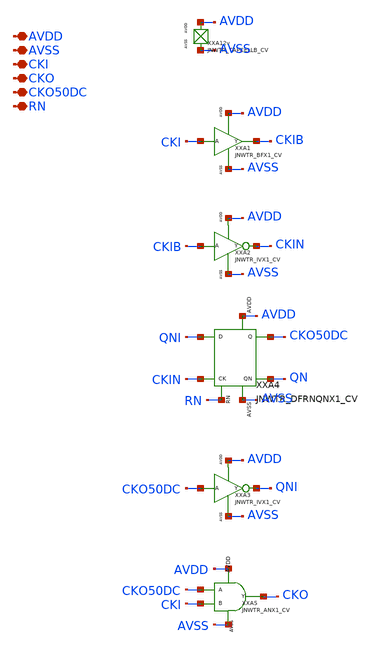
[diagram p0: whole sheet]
** sch_path: design/JNW_TR_SKY130A/JNWTR_CKDIV2_CV.sch
**.subckt JNWTR_CKDIV2_CV AVDD AVSS CKI CKO CKO50DC RN
*.iopin AVDD
*.iopin AVSS
*.iopin CKI
*.iopin CKO
*.iopin CKO50DC
*.iopin RN
XXA12v AVDD AVSS JNWTR_TAPCELLB_CV xoffset=0 yoffset=0 angle=0
XXA2 CKIB CKIN AVDD AVSS JNWTR_IVX1_CV
XXA4 QNI CKIN RN CKO50DC QN AVDD AVSS JNWTR_DFRNQNX1_CV xoffset=0 yoffset=0 angle=0
XXA3 CKO50DC QNI AVDD AVSS JNWTR_IVX1_CV
XXA5 CKO50DC CKI CKO AVDD AVSS JNWTR_ANX1_CV xoffset=0 yoffset=0 angle=0 M=1
**.ends
.end
